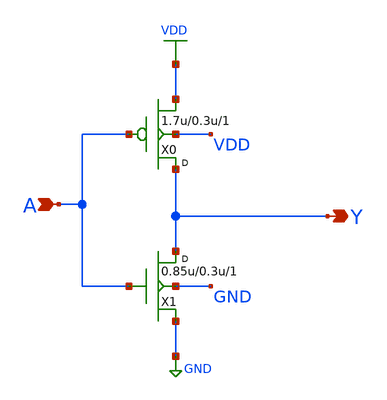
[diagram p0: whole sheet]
** sch_path: lib/xschem/gf180mcu_osu_sc_12T_inv_1.sch
**.subckt gf180mcu_osu_sc_12T_inv_1 A Y
*.ipin A
*.opin Y
X0 Y A VDD VDD pmos_3p3 w=1.7u l=0.3u m=1
X1 Y A GND GND nmos_3p3 w=0.85u l=0.3u m=1
**** begin user architecture code


.inc "/import/yukari1/lrburle/OSU_180/char/techfiles/design.hspice"
.lib "/import/yukari1/lrburle/OSU_180/char/techfiles/sm141064.hspice" typical


**** end user architecture code
**.ends
.GLOBAL VDD
.GLOBAL GND
.end
